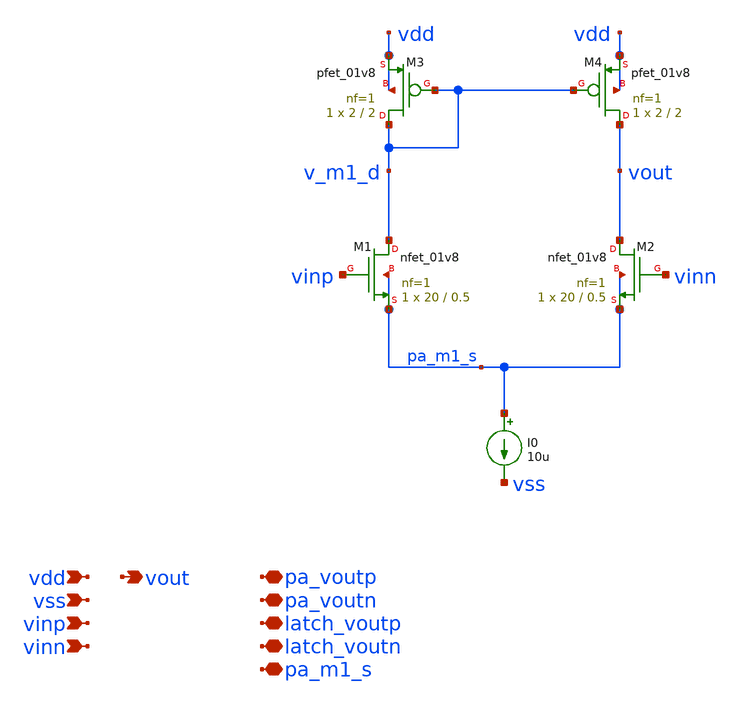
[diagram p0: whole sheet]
** sch_path: schematics/comp_5t.sch
**.subckt comp_5t vdd vout vss vinp vinn pa_voutp pa_voutn latch_voutp latch_voutn pa_m1_s
*.ipin vdd
*.opin vout
*.ipin vss
*.ipin vinp
*.ipin vinn
*.iopin pa_voutp
*.iopin pa_voutn
*.iopin latch_voutp
*.iopin latch_voutn
*.iopin pa_m1_s
I0 pa_m1_s vss 10u
XM1 v_m1_d vinp pa_m1_s pa_m1_s sky130_fd_pr__nfet_01v8 L=0.5 W=20 nf=1 ad='int((1 + 1)/2) * 20 / 1 * 0.29'
+ as='int((1 + 2)/2) * 20 / 1 * 0.29' pd='2*int((1 + 1)/2) * (20 / 1 + 0.29)' ps='2*int((1 + 2)/2) * (20 / 1 + 0.29)'
+ nrd='0.29 / 20 ' nrs='0.29 / 20 ' sa=0 sb=0 sd=0 mult=1 m=1
XM2 vout vinn pa_m1_s pa_m1_s sky130_fd_pr__nfet_01v8 L=0.5 W=20 nf=1 ad='int((1 + 1)/2) * 20 / 1 * 0.29'
+ as='int((1 + 2)/2) * 20 / 1 * 0.29' pd='2*int((1 + 1)/2) * (20 / 1 + 0.29)' ps='2*int((1 + 2)/2) * (20 / 1 + 0.29)'
+ nrd='0.29 / 20 ' nrs='0.29 / 20 ' sa=0 sb=0 sd=0 mult=1 m=1
XM3 v_m1_d v_m1_d vdd vdd sky130_fd_pr__pfet_01v8 L=2 W=2 nf=1 ad='int((1 + 1)/2) * 2 / 1 * 0.29' as='int((1 + 2)/2) * 2 / 1 * 0.29'
+ pd='2*int((1 + 1)/2) * (2 / 1 + 0.29)' ps='2*int((1 + 2)/2) * (2 / 1 + 0.29)' nrd='0.29 / 2 ' nrs='0.29 / 2 '
+ sa=0 sb=0 sd=0 mult=1 m=1
XM4 vout v_m1_d vdd vdd sky130_fd_pr__pfet_01v8 L=2 W=2 nf=1 ad='int((1 + 1)/2) * 2 / 1 * 0.29' as='int((1 + 2)/2) * 2 / 1 * 0.29'
+ pd='2*int((1 + 1)/2) * (2 / 1 + 0.29)' ps='2*int((1 + 2)/2) * (2 / 1 + 0.29)' nrd='0.29 / 2 ' nrs='0.29 / 2 '
+ sa=0 sb=0 sd=0 mult=1 m=1
**.ends
.end
